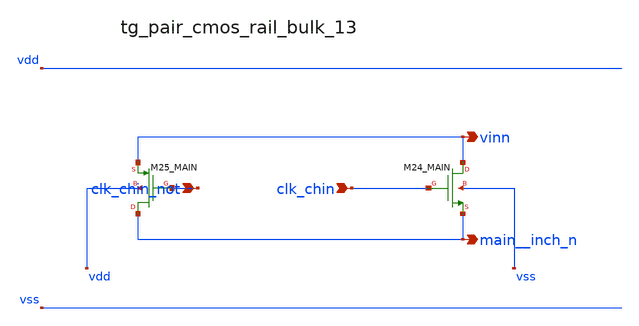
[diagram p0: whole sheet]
** sch_path: analog-db/raw/ia_004_fan_chopper_rrl/hier/blocks/tg_pair_cmos_rail_bulk_13.sch
**.subckt tg_pair_cmos_rail_bulk_13 clk_chin_not clk_chin vinn main__inch_n
*.ipin clk_chin_not
*.ipin clk_chin
*.opin vinn
*.opin main__inch_n
XM24_MAIN vinn clk_chin main__inch_n vss sg13_lv_nmos w=x_dut_xm24_main_w l=x_dut_xm24_main_l ng=1
+ m=x_dut_xm24_main_m
XM25_MAIN main__inch_n clk_chin_not vinn vdd sg13_lv_pmos w=x_dut_xm25_main_w l=x_dut_xm25_main_l
+ ng=1 m=x_dut_xm25_main_m
**.ends
.end
